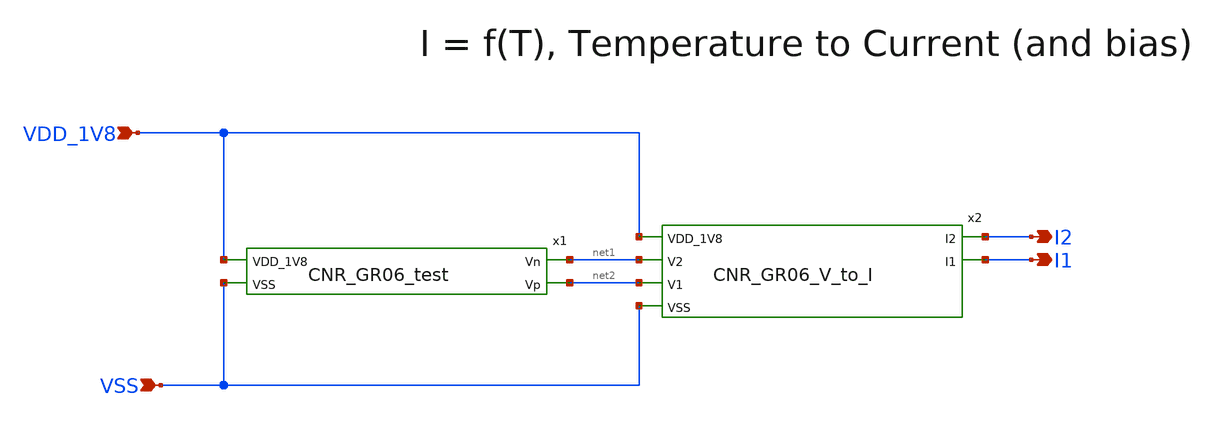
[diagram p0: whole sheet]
** sch_path: design/CNR_GR06_SKY130NM/CNR_GR06.sch
**.subckt CNR_GR06 VDD_1V8 VSS I2 I1
*.ipin VDD_1V8
*.ipin VSS
*.opin I2
*.opin I1
x1 VDD_1V8 net1 net2 VSS CNR_GR06_test
x2 VDD_1V8 I2 I1 net1 net2 VSS CNR_GR06_V_to_I
**.ends

* expanding   symbol:  CNR_GR06_SKY130NM/CNR_GR06_test.sym # of pins=4
** sym_path: design/CNR_GR06_SKY130NM/CNR_GR06_test.sym
** sch_path: design/CNR_GR06_SKY130NM/CNR_GR06_test.sch
.subckt CNR_GR06_test VDD_1V8 Vn Vp VSS
*.ipin VDD_1V8
*.ipin VSS
*.opin Vn
*.opin Vp
XM1 net6 net5 VSS GND sky130_fd_pr__nfet_01v8 L=0.15 W=1 nf=1 ad='int((nf+1)/2) * W/nf * 0.29' as='int((nf+2)/2) * W/nf * 0.29'
+ pd='2*int((nf+1)/2) * (W/nf + 0.29)' ps='2*int((nf+2)/2) * (W/nf + 0.29)' nrd='0.29 / W' nrs='0.29 / W'
+ sa=0 sb=0 sd=0 mult=1 m=1
XM3 net4 net4 VSS GND sky130_fd_pr__nfet_01v8 L=0.15 W=1 nf=1 ad='int((nf+1)/2) * W/nf * 0.29' as='int((nf+2)/2) * W/nf * 0.29'
+ pd='2*int((nf+1)/2) * (W/nf + 0.29)' ps='2*int((nf+2)/2) * (W/nf + 0.29)' nrd='0.29 / W' nrs='0.29 / W'
+ sa=0 sb=0 sd=0 mult=1 m=1
XM4 net3 net4 VSS GND sky130_fd_pr__nfet_01v8 L=0.15 W=1 nf=1 ad='int((nf+1)/2) * W/nf * 0.29' as='int((nf+2)/2) * W/nf * 0.29'
+ pd='2*int((nf+1)/2) * (W/nf + 0.29)' ps='2*int((nf+2)/2) * (W/nf + 0.29)' nrd='0.29 / W' nrs='0.29 / W'
+ sa=0 sb=0 sd=0 mult=1 m=1
XM5 net2 net11 net12 GND sky130_fd_pr__nfet_01v8 L=0.15 W=1 nf=1 ad='int((nf+1)/2) * W/nf * 0.29' as='int((nf+2)/2) * W/nf * 0.29'
+ pd='2*int((nf+1)/2) * (W/nf + 0.29)' ps='2*int((nf+2)/2) * (W/nf + 0.29)' nrd='0.29 / W' nrs='0.29 / W'
+ sa=0 sb=0 sd=0 mult=1 m=1
XM6 net11 net11 VSS GND sky130_fd_pr__nfet_01v8 L=0.15 W=1 nf=1 ad='int((nf+1)/2) * W/nf * 0.29' as='int((nf+2)/2) * W/nf * 0.29'
+ pd='2*int((nf+1)/2) * (W/nf + 0.29)' ps='2*int((nf+2)/2) * (W/nf + 0.29)' nrd='0.29 / W' nrs='0.29 / W'
+ sa=0 sb=0 sd=0 mult=1 m=1
XM11 net5 net5 net6 GND sky130_fd_pr__nfet_01v8 L=0.15 W=1 nf=1 ad='int((nf+1)/2) * W/nf * 0.29' as='int((nf+2)/2) * W/nf * 0.29'
+ pd='2*int((nf+1)/2) * (W/nf + 0.29)' ps='2*int((nf+2)/2) * (W/nf + 0.29)' nrd='0.29 / W' nrs='0.29 / W'
+ sa=0 sb=0 sd=0 mult=1 m=1
XM12 Vn Vn net6 GND sky130_fd_pr__nfet_01v8 L=0.15 W=1 nf=1 ad='int((nf+1)/2) * W/nf * 0.29' as='int((nf+2)/2) * W/nf * 0.29'
+ pd='2*int((nf+1)/2) * (W/nf + 0.29)' ps='2*int((nf+2)/2) * (W/nf + 0.29)' nrd='0.29 / W' nrs='0.29 / W'
+ sa=0 sb=0 sd=0 mult=1 m=1
XM17 net10 net9 VSS GND sky130_fd_pr__nfet_01v8 L=0.15 W=1 nf=1 ad='int((nf+1)/2) * W/nf * 0.29' as='int((nf+2)/2) * W/nf * 0.29'
+ pd='2*int((nf+1)/2) * (W/nf + 0.29)' ps='2*int((nf+2)/2) * (W/nf + 0.29)' nrd='0.29 / W' nrs='0.29 / W'
+ sa=0 sb=0 sd=0 mult=1 m=1
XM18 Vp net9 VSS GND sky130_fd_pr__nfet_01v8 L=0.15 W=1 nf=1 ad='int((nf+1)/2) * W/nf * 0.29' as='int((nf+2)/2) * W/nf * 0.29'
+ pd='2*int((nf+1)/2) * (W/nf + 0.29)' ps='2*int((nf+2)/2) * (W/nf + 0.29)' nrd='0.29 / W' nrs='0.29 / W'
+ sa=0 sb=0 sd=0 mult=1 m=1
XM8 VDD_1V8 net1 net11 GND sky130_fd_pr__nfet_01v8 L=0.15 W=1 nf=1 ad='int((nf+1)/2) * W/nf * 0.29' as='int((nf+2)/2) * W/nf * 0.29'
+ pd='2*int((nf+1)/2) * (W/nf + 0.29)' ps='2*int((nf+2)/2) * (W/nf + 0.29)' nrd='0.29 / W' nrs='0.29 / W'
+ sa=0 sb=0 sd=0 mult=1 m=1
XM7 VDD_1V8 net1 net2 GND sky130_fd_pr__nfet_01v8 L=0.15 W=1 nf=1 ad='int((nf+1)/2) * W/nf * 0.29' as='int((nf+2)/2) * W/nf * 0.29'
+ pd='2*int((nf+1)/2) * (W/nf + 0.29)' ps='2*int((nf+2)/2) * (W/nf + 0.29)' nrd='0.29 / W' nrs='0.29 / W'
+ sa=0 sb=0 sd=0 mult=1 m=1
XM2 VDD_1V8 net1 net4 GND sky130_fd_pr__nfet_01v8 L=0.15 W=1 nf=1 ad='int((nf+1)/2) * W/nf * 0.29' as='int((nf+2)/2) * W/nf * 0.29'
+ pd='2*int((nf+1)/2) * (W/nf + 0.29)' ps='2*int((nf+2)/2) * (W/nf + 0.29)' nrd='0.29 / W' nrs='0.29 / W'
+ sa=0 sb=0 sd=0 mult=1 m=1
XM10 VDD_1V8 net1 net5 GND sky130_fd_pr__nfet_01v8 L=0.15 W=1 nf=1 ad='int((nf+1)/2) * W/nf * 0.29' as='int((nf+2)/2) * W/nf * 0.29'
+ pd='2*int((nf+1)/2) * (W/nf + 0.29)' ps='2*int((nf+2)/2) * (W/nf + 0.29)' nrd='0.29 / W' nrs='0.29 / W'
+ sa=0 sb=0 sd=0 mult=1 m=1
XM9 VDD_1V8 net1 Vn GND sky130_fd_pr__nfet_01v8 L=0.15 W=1 nf=1 ad='int((nf+1)/2) * W/nf * 0.29' as='int((nf+2)/2) * W/nf * 0.29'
+ pd='2*int((nf+1)/2) * (W/nf + 0.29)' ps='2*int((nf+2)/2) * (W/nf + 0.29)' nrd='0.29 / W' nrs='0.29 / W'
+ sa=0 sb=0 sd=0 mult=1 m=1
XM13 VDD_1V8 net8 net7 GND sky130_fd_pr__nfet_01v8 L=0.15 W=1 nf=1 ad='int((nf+1)/2) * W/nf * 0.29' as='int((nf+2)/2) * W/nf * 0.29'
+ pd='2*int((nf+1)/2) * (W/nf + 0.29)' ps='2*int((nf+2)/2) * (W/nf + 0.29)' nrd='0.29 / W' nrs='0.29 / W'
+ sa=0 sb=0 sd=0 mult=1 m=1
XM15 net7 Vp Vp GND sky130_fd_pr__nfet_01v8 L=0.15 W=1 nf=1 ad='int((nf+1)/2) * W/nf * 0.29' as='int((nf+2)/2) * W/nf * 0.29'
+ pd='2*int((nf+1)/2) * (W/nf + 0.29)' ps='2*int((nf+2)/2) * (W/nf + 0.29)' nrd='0.29 / W' nrs='0.29 / W'
+ sa=0 sb=0 sd=0 mult=1 m=1
XM14 net7 net8 net8 GND sky130_fd_pr__nfet_01v8 L=0.15 W=1 nf=1 ad='int((nf+1)/2) * W/nf * 0.29' as='int((nf+2)/2) * W/nf * 0.29'
+ pd='2*int((nf+1)/2) * (W/nf + 0.29)' ps='2*int((nf+2)/2) * (W/nf + 0.29)' nrd='0.29 / W' nrs='0.29 / W'
+ sa=0 sb=0 sd=0 mult=1 m=1
XM16 net8 Vp net10 GND sky130_fd_pr__nfet_01v8 L=0.15 W=1 nf=1 ad='int((nf+1)/2) * W/nf * 0.29' as='int((nf+2)/2) * W/nf * 0.29'
+ pd='2*int((nf+1)/2) * (W/nf + 0.29)' ps='2*int((nf+2)/2) * (W/nf + 0.29)' nrd='0.29 / W' nrs='0.29 / W'
+ sa=0 sb=0 sd=0 mult=1 m=1
.ends


* expanding   symbol:  CNR_GR06_SKY130NM/CNR_GR06_V_to_I.sym # of pins=6
** sym_path: design/CNR_GR06_SKY130NM/CNR_GR06_V_to_I.sym
** sch_path: design/CNR_GR06_SKY130NM/CNR_GR06_V_to_I.sch
.subckt CNR_GR06_V_to_I VDD_1V8 I2 I1 V2 V1 VSS
*.ipin VDD_1V8
*.ipin VSS
*.opin I1
*.opin I2
*.ipin V1
*.ipin V2
XM6 VDD_1V8 net1 net1 GND sky130_fd_pr__nfet_01v8 L=0.15 W=1 nf=1 ad='int((nf+1)/2) * W/nf * 0.29' as='int((nf+2)/2) * W/nf * 0.29'
+ pd='2*int((nf+1)/2) * (W/nf + 0.29)' ps='2*int((nf+2)/2) * (W/nf + 0.29)' nrd='0.29 / W' nrs='0.29 / W'
+ sa=0 sb=0 sd=0 mult=1 m=1
XM1 VDD_1V8 net1 I1 GND sky130_fd_pr__nfet_01v8 L=0.15 W=1 nf=1 ad='int((nf+1)/2) * W/nf * 0.29' as='int((nf+2)/2) * W/nf * 0.29'
+ pd='2*int((nf+1)/2) * (W/nf + 0.29)' ps='2*int((nf+2)/2) * (W/nf + 0.29)' nrd='0.29 / W' nrs='0.29 / W'
+ sa=0 sb=0 sd=0 mult=1 m=1
XM2 VDD_1V8 net2 net2 GND sky130_fd_pr__nfet_01v8 L=0.15 W=1 nf=1 ad='int((nf+1)/2) * W/nf * 0.29' as='int((nf+2)/2) * W/nf * 0.29'
+ pd='2*int((nf+1)/2) * (W/nf + 0.29)' ps='2*int((nf+2)/2) * (W/nf + 0.29)' nrd='0.29 / W' nrs='0.29 / W'
+ sa=0 sb=0 sd=0 mult=1 m=1
XM3 VDD_1V8 net2 I2 GND sky130_fd_pr__nfet_01v8 L=0.15 W=1 nf=1 ad='int((nf+1)/2) * W/nf * 0.29' as='int((nf+2)/2) * W/nf * 0.29'
+ pd='2*int((nf+1)/2) * (W/nf + 0.29)' ps='2*int((nf+2)/2) * (W/nf + 0.29)' nrd='0.29 / W' nrs='0.29 / W'
+ sa=0 sb=0 sd=0 mult=1 m=1
XM4 net2 V2 VSS GND sky130_fd_pr__nfet_01v8 L=0.15 W=1 nf=1 ad='int((nf+1)/2) * W/nf * 0.29' as='int((nf+2)/2) * W/nf * 0.29'
+ pd='2*int((nf+1)/2) * (W/nf + 0.29)' ps='2*int((nf+2)/2) * (W/nf + 0.29)' nrd='0.29 / W' nrs='0.29 / W'
+ sa=0 sb=0 sd=0 mult=1 m=1
XM5 net1 V1 VSS GND sky130_fd_pr__nfet_01v8 L=0.15 W=1 nf=1 ad='int((nf+1)/2) * W/nf * 0.29' as='int((nf+2)/2) * W/nf * 0.29'
+ pd='2*int((nf+1)/2) * (W/nf + 0.29)' ps='2*int((nf+2)/2) * (W/nf + 0.29)' nrd='0.29 / W' nrs='0.29 / W'
+ sa=0 sb=0 sd=0 mult=1 m=1
.ends

.end
